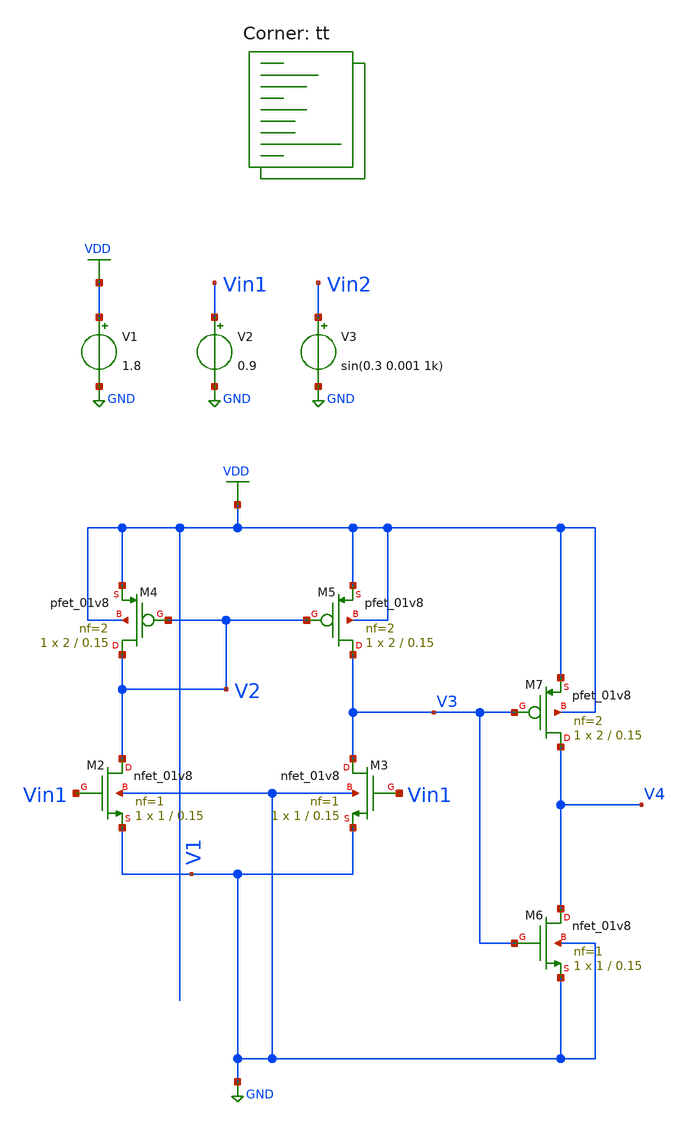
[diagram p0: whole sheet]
** sch_path: projects/pll/charge_pump/xschem_ngspice/tb_opamp.sch
**.subckt tb_opamp
V1 VDD GND 1.8
V2 Vin1 GND 0.9
V3 Vin2 GND sin(0.3 0.001 1k)
XM2 V2 Vin1 GND GND sky130_fd_pr__nfet_01v8 L=0.15 W=1 nf=1 ad='int((nf+1)/2) * W/nf * 0.29' as='int((nf+2)/2) * W/nf * 0.29'
+ pd='2*int((nf+1)/2) * (W/nf + 0.29)' ps='2*int((nf+2)/2) * (W/nf + 0.29)' nrd='0.29 / W' nrs='0.29 / W'
+ sa=0 sb=0 sd=0 mult=1 m=1
XM3 V3 Vin1 GND GND sky130_fd_pr__nfet_01v8 L=0.15 W=1 nf=1 ad='int((nf+1)/2) * W/nf * 0.29' as='int((nf+2)/2) * W/nf * 0.29'
+ pd='2*int((nf+1)/2) * (W/nf + 0.29)' ps='2*int((nf+2)/2) * (W/nf + 0.29)' nrd='0.29 / W' nrs='0.29 / W'
+ sa=0 sb=0 sd=0 mult=1 m=1
XM4 V2 V2 VDD VDD sky130_fd_pr__pfet_01v8 L=0.15 W=2 nf=2 ad='int((nf+1)/2) * W/nf * 0.29' as='int((nf+2)/2) * W/nf * 0.29'
+ pd='2*int((nf+1)/2) * (W/nf + 0.29)' ps='2*int((nf+2)/2) * (W/nf + 0.29)' nrd='0.29 / W' nrs='0.29 / W'
+ sa=0 sb=0 sd=0 mult=1 m=1
XM5 V3 V2 VDD VDD sky130_fd_pr__pfet_01v8 L=0.15 W=2 nf=2 ad='int((nf+1)/2) * W/nf * 0.29' as='int((nf+2)/2) * W/nf * 0.29'
+ pd='2*int((nf+1)/2) * (W/nf + 0.29)' ps='2*int((nf+2)/2) * (W/nf + 0.29)' nrd='0.29 / W' nrs='0.29 / W'
+ sa=0 sb=0 sd=0 mult=1 m=1
XM6 V4 V3 GND GND sky130_fd_pr__nfet_01v8 L=0.15 W=1 nf=1 ad='int((nf+1)/2) * W/nf * 0.29' as='int((nf+2)/2) * W/nf * 0.29'
+ pd='2*int((nf+1)/2) * (W/nf + 0.29)' ps='2*int((nf+2)/2) * (W/nf + 0.29)' nrd='0.29 / W' nrs='0.29 / W'
+ sa=0 sb=0 sd=0 mult=1 m=1
XM7 V4 V3 VDD VDD sky130_fd_pr__pfet_01v8 L=0.15 W=2 nf=2 ad='int((nf+1)/2) * W/nf * 0.29' as='int((nf+2)/2) * W/nf * 0.29'
+ pd='2*int((nf+1)/2) * (W/nf + 0.29)' ps='2*int((nf+2)/2) * (W/nf + 0.29)' nrd='0.29 / W' nrs='0.29 / W'
+ sa=0 sb=0 sd=0 mult=1 m=1
**** begin user architecture code



.option wnflag=1
.option savecurrents

* .param VDDGAUSS = agauss(1.8, 0.05, 1)
* .param VDD = VDDGAUSS
* .param VDD = 1.8

* .param TEMPGAUSS = agauss(40, 30, 1)
* .param temp = TEMPGAUSS
* .option temp = 26

.save @m.xm1.msky130_fd_pr__nfet_01v8[gm] @m.xm2.msky130_fd_pr__nfet_01v8[gm] @m.xm3.msky130_fd_pr__nfet_01v8[gm] @m.xm4.msky130_fd_pr__pfet_01v8[gm] @m.xm5.msky130_fd_pr__pfet_01v8[gm]


.control

  save all
  *tran 1u 20m
  * ac dec 20 1 1T
  dc v2 0 1.8 0.001

  write tb_opamp.raw
  set appendwrite

.endc



.lib $::SKYWATER_MODELS/sky130.lib.spice tt
**** end user architecture code
**.ends
.GLOBAL GND
.GLOBAL VDD
.end
